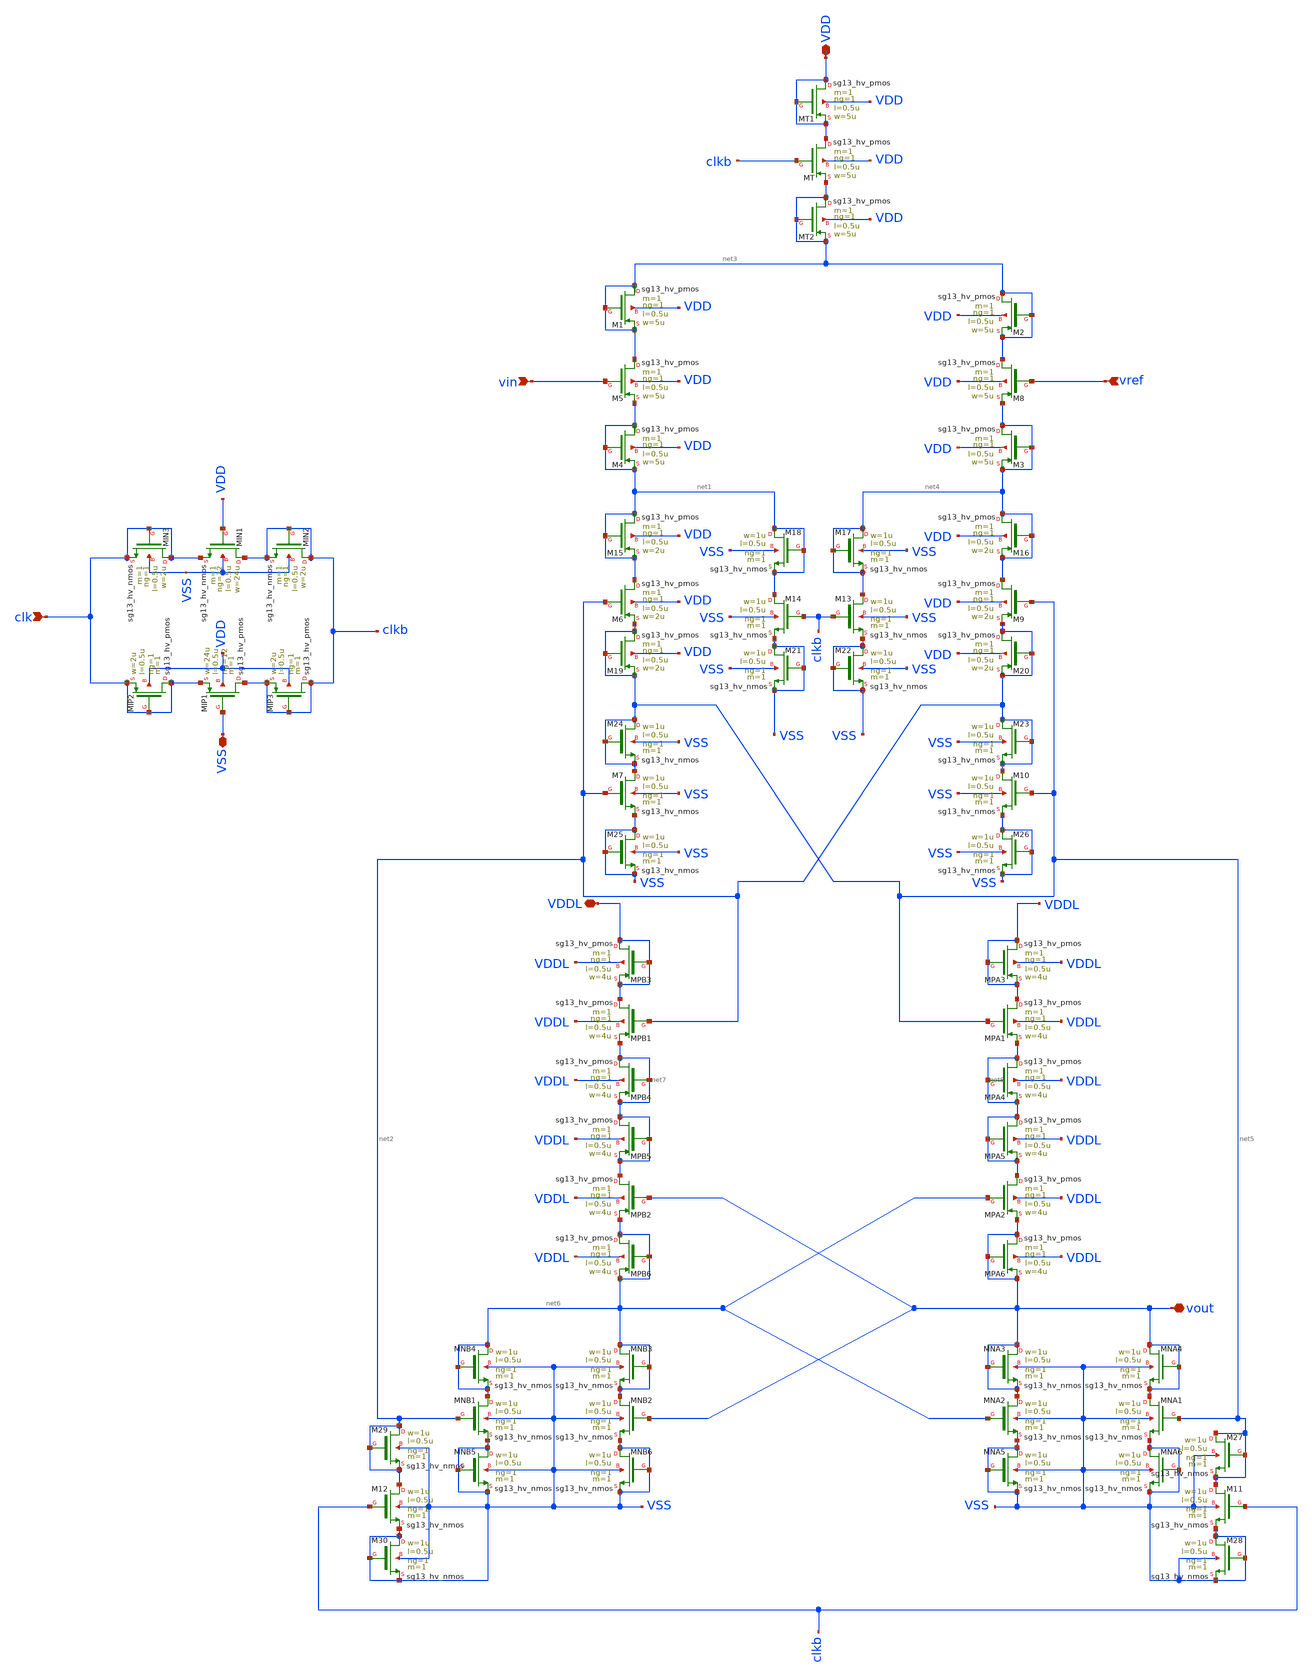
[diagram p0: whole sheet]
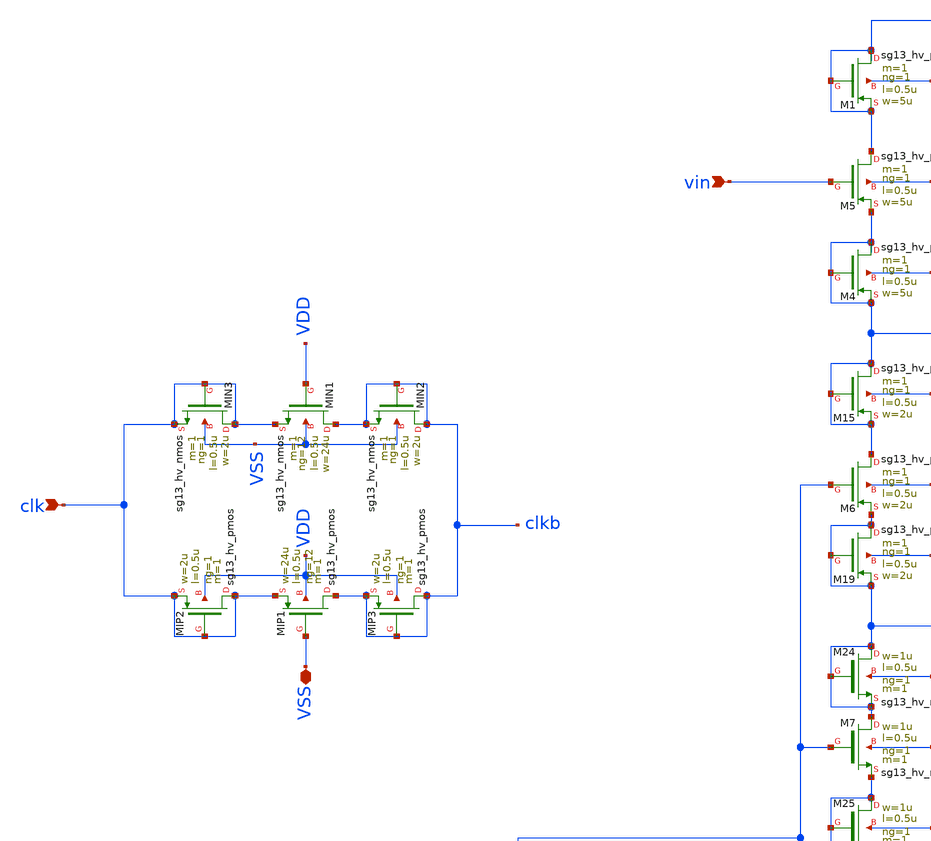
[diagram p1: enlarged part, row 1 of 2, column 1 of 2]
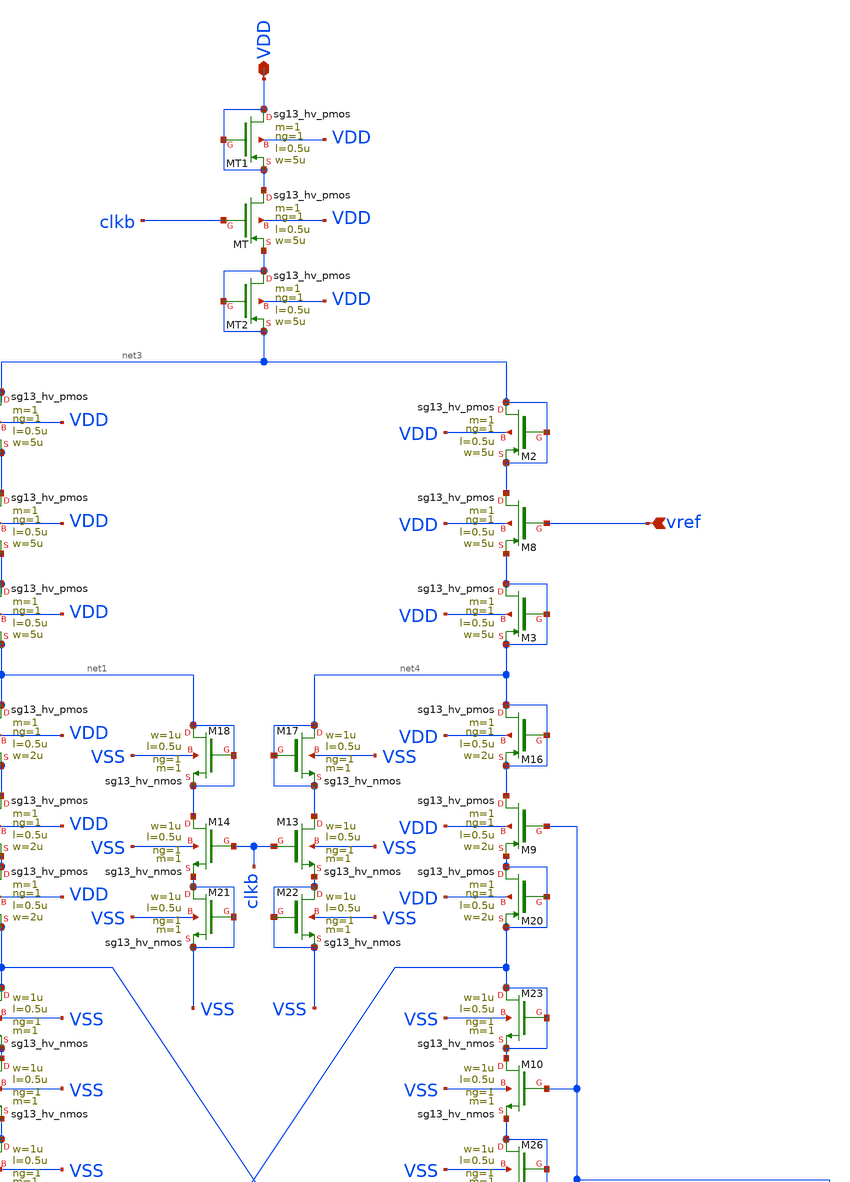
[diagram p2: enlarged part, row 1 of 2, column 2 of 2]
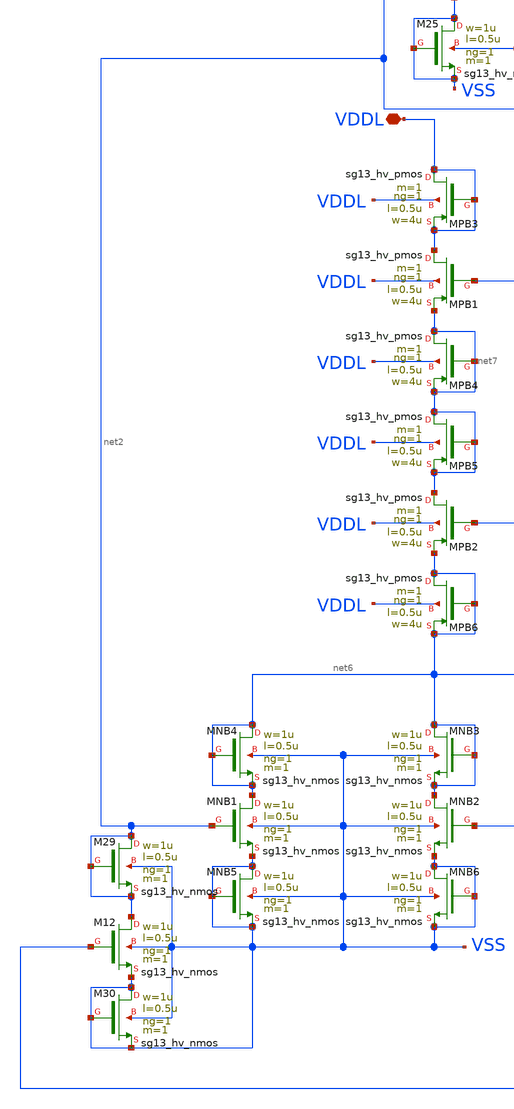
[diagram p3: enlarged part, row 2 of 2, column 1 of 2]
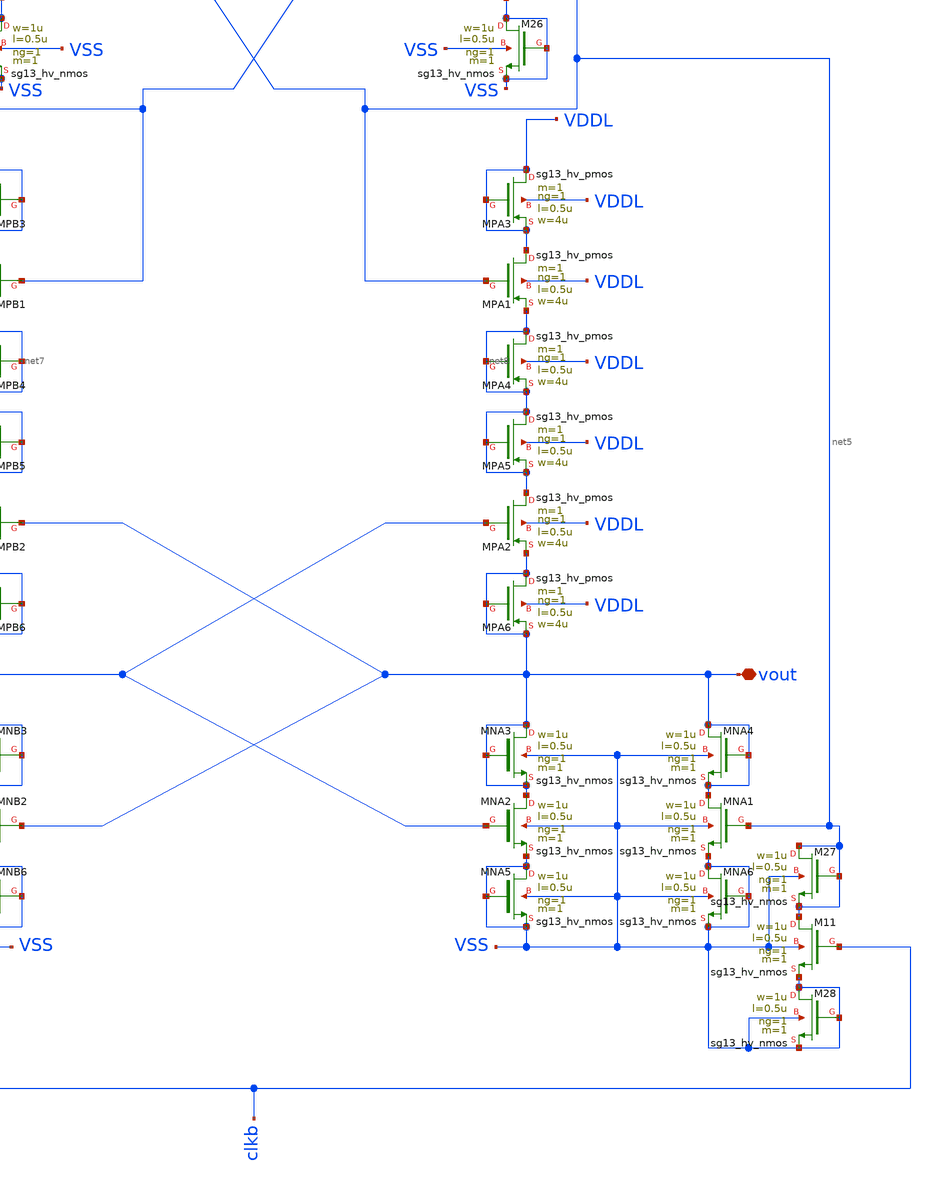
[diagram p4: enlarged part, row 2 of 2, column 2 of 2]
** sch_path: macros/heichips26_ook/macros/ook_analog_system/schematic/xschem/stash/clocked_comparator.sch
**.subckt clocked_comparator VDD VDDL vin vref vout clk VSS
*.iopin VDD
*.iopin VDDL
*.ipin vin
*.ipin vref
*.iopin vout
*.ipin clk
*.iopin VSS
XMT VDD clkb net3 VDD sg13_hv_pmos w=5u l=0.5u ng=1 m=1 mm_ok=1
XM5 net3 vin net1 VDD sg13_hv_pmos w=5u l=0.5u ng=1 m=1 mm_ok=1
XM6 net1 net2 net5 VDD sg13_hv_pmos w=2u l=0.5u ng=1 m=1 mm_ok=1
XM7 net5 net2 VSS VSS sg13_hv_nmos w=1u l=0.5u ng=1 m=1 mm_ok=1
XM8 net3 vref net4 VDD sg13_hv_pmos w=5u l=0.5u ng=1 m=1 mm_ok=1
XM9 net4 net5 net2 VDD sg13_hv_pmos w=2u l=0.5u ng=1 m=1 mm_ok=1
XM10 net2 net5 VSS VSS sg13_hv_nmos w=1u l=0.5u ng=1 m=1 mm_ok=1
XM11 net5 clkb VSS VSS sg13_hv_nmos w=1u l=0.5u ng=1 m=1 mm_ok=1
XM12 net2 clkb VSS VSS sg13_hv_nmos w=1u l=0.5u ng=1 m=1 mm_ok=1
XM13 net4 clkb VSS VSS sg13_hv_nmos w=1u l=0.5u ng=1 m=1 mm_ok=1
XMPA1 VDDL net5 net8 VDDL sg13_hv_pmos w=4u l=0.5u ng=1 m=1 mm_ok=1
XMPA2 net8 net6 vout VDDL sg13_hv_pmos w=4u l=0.5u ng=1 m=1 mm_ok=1
XMNA1 vout net5 VSS VSS sg13_hv_nmos w=1u l=0.5u ng=1 m=1 mm_ok=1
XMNA2 vout net6 VSS VSS sg13_hv_nmos w=1u l=0.5u ng=1 m=1 mm_ok=1
XMPB1 VDDL net2 net7 VDDL sg13_hv_pmos w=4u l=0.5u ng=1 m=1 mm_ok=1
XMPB2 net7 vout net6 VDDL sg13_hv_pmos w=4u l=0.5u ng=1 m=1 mm_ok=1
XMNB1 net6 net2 VSS VSS sg13_hv_nmos w=1u l=0.5u ng=1 m=1 mm_ok=1
XMNB2 net6 vout VSS VSS sg13_hv_nmos w=1u l=0.5u ng=1 m=1 mm_ok=1
XM14 net1 clkb VSS VSS sg13_hv_nmos w=1u l=0.5u ng=1 m=1 mm_ok=1
XMIP1 clkb VSS clk VDD sg13_hv_pmos w=24u l=0.5u ng=12 m=1 mm_ok=1
XMIN1 clkb VDD clk VSS sg13_hv_nmos w=24u l=0.5u ng=12 m=1 mm_ok=1
XMT1 VDD VDD VDD VDD sg13_hv_pmos w=5u l=0.5u ng=1 m=1 mm_ok=1
XMT2 net3 net3 net3 VDD sg13_hv_pmos w=5u l=0.5u ng=1 m=1 mm_ok=1
XMIN2 clkb clkb clkb VSS sg13_hv_nmos w=2u l=0.5u ng=1 m=1 mm_ok=1
XMIN3 clk clk clk VSS sg13_hv_nmos w=2u l=0.5u ng=1 m=1 mm_ok=1
XMIP2 clk clk clk VDD sg13_hv_pmos w=2u l=0.5u ng=1 m=1 mm_ok=1
XMIP3 clkb clkb clkb VDD sg13_hv_pmos w=2u l=0.5u ng=1 m=1 mm_ok=1
XM1 net3 net3 net3 VDD sg13_hv_pmos w=5u l=0.5u ng=1 m=1 mm_ok=1
XM2 net3 net3 net3 VDD sg13_hv_pmos w=5u l=0.5u ng=1 m=1 mm_ok=1
XM3 net4 net4 net4 VDD sg13_hv_pmos w=5u l=0.5u ng=1 m=1 mm_ok=1
XM4 net1 net1 net1 VDD sg13_hv_pmos w=5u l=0.5u ng=1 m=1 mm_ok=1
XM15 net1 net1 net1 VDD sg13_hv_pmos w=2u l=0.5u ng=1 m=1 mm_ok=1
XM16 net4 net4 net4 VDD sg13_hv_pmos w=2u l=0.5u ng=1 m=1 mm_ok=1
XM17 net4 net4 net4 VSS sg13_hv_nmos w=1u l=0.5u ng=1 m=1 mm_ok=1
XM18 net1 net1 net1 VSS sg13_hv_nmos w=1u l=0.5u ng=1 m=1 mm_ok=1
XM19 net5 net5 net5 VDD sg13_hv_pmos w=2u l=0.5u ng=1 m=1 mm_ok=1
XM20 net2 net2 net2 VDD sg13_hv_pmos w=2u l=0.5u ng=1 m=1 mm_ok=1
XM21 VSS VSS VSS VSS sg13_hv_nmos w=1u l=0.5u ng=1 m=1 mm_ok=1
XM22 VSS VSS VSS VSS sg13_hv_nmos w=1u l=0.5u ng=1 m=1 mm_ok=1
XM23 net2 net2 net2 VSS sg13_hv_nmos w=1u l=0.5u ng=1 m=1 mm_ok=1
XM24 net5 net5 net5 VSS sg13_hv_nmos w=1u l=0.5u ng=1 m=1 mm_ok=1
XM25 VSS VSS VSS VSS sg13_hv_nmos w=1u l=0.5u ng=1 m=1 mm_ok=1
XM26 VSS VSS VSS VSS sg13_hv_nmos w=1u l=0.5u ng=1 m=1 mm_ok=1
XMPA3 VDDL VDDL VDDL VDDL sg13_hv_pmos w=4u l=0.5u ng=1 m=1 mm_ok=1
XMPB3 VDDL VDDL VDDL VDDL sg13_hv_pmos w=4u l=0.5u ng=1 m=1 mm_ok=1
XMPB4 net7 net7 net7 VDDL sg13_hv_pmos w=4u l=0.5u ng=1 m=1 mm_ok=1
XMPA4 net8 net8 net8 VDDL sg13_hv_pmos w=4u l=0.5u ng=1 m=1 mm_ok=1
XMPA5 net8 net8 net8 VDDL sg13_hv_pmos w=4u l=0.5u ng=1 m=1 mm_ok=1
XMPB5 net7 net7 net7 VDDL sg13_hv_pmos w=4u l=0.5u ng=1 m=1 mm_ok=1
XMPA6 vout vout vout VDDL sg13_hv_pmos w=4u l=0.5u ng=1 m=1 mm_ok=1
XMPB6 net6 net6 net6 VDDL sg13_hv_pmos w=4u l=0.5u ng=1 m=1 mm_ok=1
XMNA3 vout vout vout VSS sg13_hv_nmos w=1u l=0.5u ng=1 m=1 mm_ok=1
XMNA4 vout vout vout VSS sg13_hv_nmos w=1u l=0.5u ng=1 m=1 mm_ok=1
XMNB3 net6 net6 net6 VSS sg13_hv_nmos w=1u l=0.5u ng=1 m=1 mm_ok=1
XMNB4 net6 net6 net6 VSS sg13_hv_nmos w=1u l=0.5u ng=1 m=1 mm_ok=1
XMNB5 VSS VSS VSS VSS sg13_hv_nmos w=1u l=0.5u ng=1 m=1 mm_ok=1
XMNB6 VSS VSS VSS VSS sg13_hv_nmos w=1u l=0.5u ng=1 m=1 mm_ok=1
XMNA5 VSS VSS VSS VSS sg13_hv_nmos w=1u l=0.5u ng=1 m=1 mm_ok=1
XMNA6 VSS VSS VSS VSS sg13_hv_nmos w=1u l=0.5u ng=1 m=1 mm_ok=1
XM27 net5 net5 net5 VSS sg13_hv_nmos w=1u l=0.5u ng=1 m=1 mm_ok=1
XM28 VSS VSS VSS VSS sg13_hv_nmos w=1u l=0.5u ng=1 m=1 mm_ok=1
XM29 net2 net2 net2 VSS sg13_hv_nmos w=1u l=0.5u ng=1 m=1 mm_ok=1
XM30 VSS VSS VSS VSS sg13_hv_nmos w=1u l=0.5u ng=1 m=1 mm_ok=1
**.ends
.end
